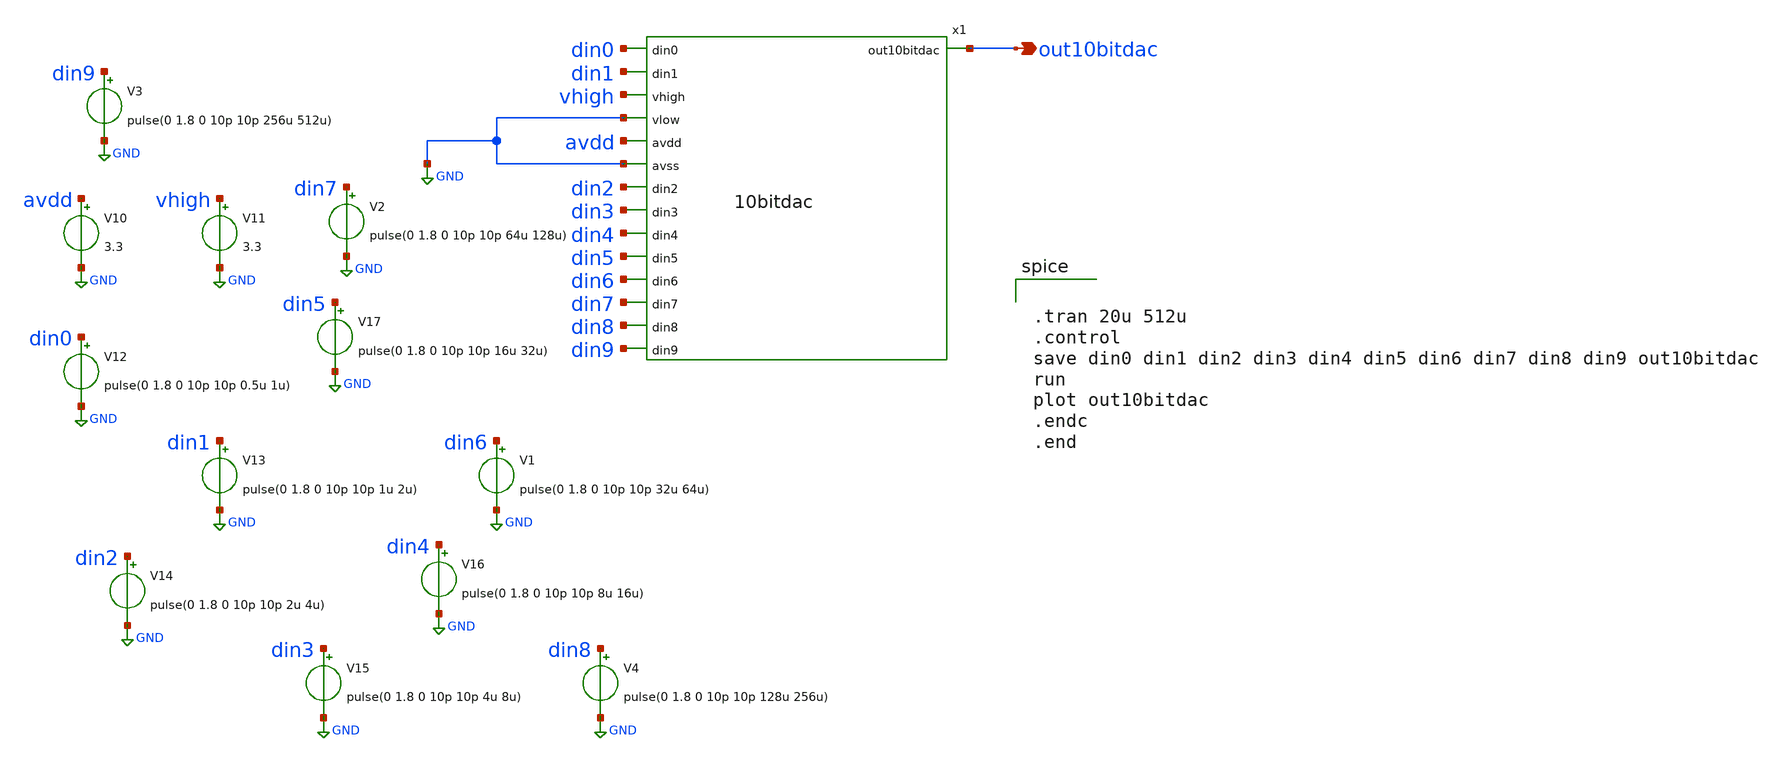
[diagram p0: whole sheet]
** sch_path: xschem/tb_10bitdac.sch
**.subckt tb_10bitdac out10bitdac
*.opin out10bitdac
x1 out10bitdac din0 din1 vhigh GND avdd GND din2 din3 din4 din5 din6 din7 din8 din9 10bitdac
V10 avdd GND 3.3
V11 vhigh GND 3.3
V12 din0 GND pulse(0 1.8 0 10p 10p 0.5u 1u)
V13 din1 GND pulse(0 1.8 0 10p 10p 1u 2u)
V14 din2 GND pulse(0 1.8 0 10p 10p 2u 4u)
V15 din3 GND pulse(0 1.8 0 10p 10p 4u 8u)
V16 din4 GND pulse(0 1.8 0 10p 10p 8u 16u)
V17 din5 GND pulse(0 1.8 0 10p 10p 16u 32u)
V1 din6 GND pulse(0 1.8 0 10p 10p 32u 64u)
V2 din7 GND pulse(0 1.8 0 10p 10p 64u 128u)
V3 din9 GND pulse(0 1.8 0 10p 10p 256u 512u)
V4 din8 GND pulse(0 1.8 0 10p 10p 128u 256u)
**** begin user architecture code

** opencircuitdesign pdks install
.lib $::SKYWATER_MODELS/sky130.lib.spice tt




.tran 20u 512u
.control
save din0 din1 din2 din3 din4 din5 din6 din7 din8 din9 out10bitdac
run
plot out10bitdac
.endc
.end

**** end user architecture code
**.ends
.GLOBAL GND
.end
